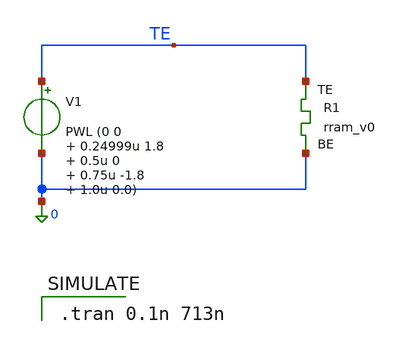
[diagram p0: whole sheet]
** sch_path: memristor_models/wellposed/tb_lissajous.sch
**.subckt tb_lissajous
V1 TE 0 PWL (0 0 0.24999u 1.8 0.5u 0 0.75u -1.8 1.0u 0.0)
XR1 TE 0 rram_v0
**** begin user architecture code

.tran 0.1n 713n


** opencircuitdesign pdks install
.inc $::SKYWATER_MODELS/rram_v0.spice


.control
save all
run
write tb_lissajous.raw
.endc



**** end user architecture code
**.ends
.end
